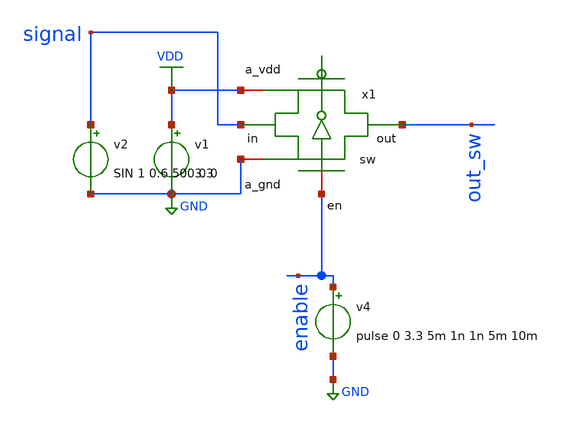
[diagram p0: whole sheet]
** sch_path: Schematics/ADC/simulations_elements/sim_sw_sinewave.sch
**.subckt sim_sw_sinewave
x1 GND VDD enable signal out_sw sw
v1 VDD GND 3.3
v4 enable GND pulse 0 3.3 5m 1n 1n 5m 10m
v2 signal GND SIN 1 0.6 500 0 0
**** begin user architecture code

** opencircuitdesign pdks install
.lib $::SKYWATER_MODELS/sky130.lib.spice tt

**** end user architecture code
**.ends
.GLOBAL GND
.GLOBAL VDD
**** begin user architecture code

* .option SCALE=1e-6
.option method=gear seed=12
.control
save all
tran 0.1m 30m
write sim_sw_sinewave.raw
plot enable out_sw
.endc


**** end user architecture code
.end
